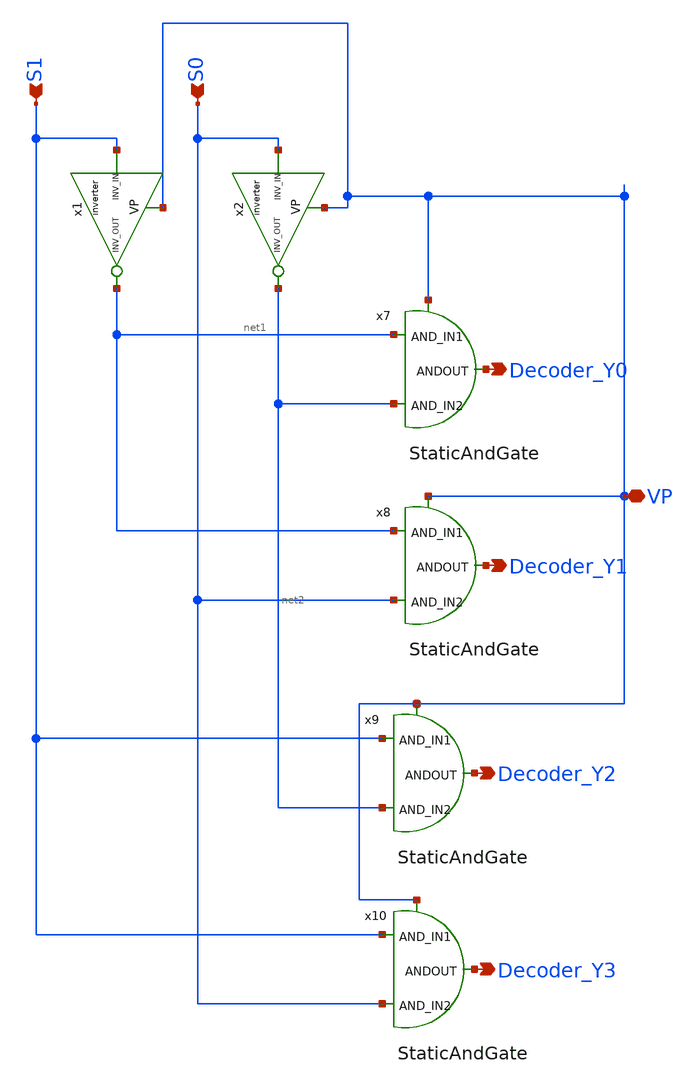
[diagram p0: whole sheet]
** sch_path: AllSymbols&Sch/Decoder/Decoder_2:4.sch
**.subckt Decoder_2:4 S0 Decoder_Y0 VP S1 Decoder_Y1 Decoder_Y2 Decoder_Y3
*.ipin S0
*.opin Decoder_Y0
*.iopin VP
*.ipin S1
*.opin Decoder_Y1
*.opin Decoder_Y2
*.opin Decoder_Y3
x7 Decoder_Y0 net1 net2 VP StaticAndGate
x8 Decoder_Y1 net1 S0 VP StaticAndGate
x9 Decoder_Y2 S1 net2 VP StaticAndGate
x10 Decoder_Y3 S1 S0 VP StaticAndGate
x1 VP net1 S1 inverter
x2 VP net2 S0 inverter
**.ends

* expanding   symbol:
*+  /home/safal/projects/GitHub_CMOS_4bit_ALU/AllSymbols&Sch/Gates/StaticAndGate.sym # of pins=4
** sym_path: AllSymbols&Sch/Gates/StaticAndGate.sym
** sch_path: AllSymbols&Sch/Gates/StaticAndGate.sch
.subckt StaticAndGate ANDOUT AND_IN1 AND_IN2 VP
*.ipin AND_IN1
*.opin ANDOUT
*.ipin AND_IN2
*.iopin VP
XM1 net2 AND_IN2 VP VP sky130_fd_pr__pfet_01v8 L=0.15 W=1 nf=1 ad='int((1 + 1)/2) * 1 / 1 * 0.29' as='int((1 + 2)/2) * 1 / 1 * 0.29'
+ pd='2*int((1 + 1)/2) * (1 / 1 + 0.29)' ps='2*int((1 + 2)/2) * (1 / 1 + 0.29)' nrd='0.29 / 1 ' nrs='0.29 / 1 '
+ sa=0 sb=0 sd=0 mult=1 m=1
XM2 net2 AND_IN1 net1 net1 sky130_fd_pr__nfet_01v8 L=0.15 W=2 nf=1 ad='int((1 + 1)/2) * 2 / 1 * 0.29'
+ as='int((1 + 2)/2) * 2 / 1 * 0.29' pd='2*int((1 + 1)/2) * (2 / 1 + 0.29)' ps='2*int((1 + 2)/2) * (2 / 1 + 0.29)'
+ nrd='0.29 / 2 ' nrs='0.29 / 2 ' sa=0 sb=0 sd=0 mult=1 m=1
XM3 net1 AND_IN2 GND GND sky130_fd_pr__nfet_01v8 L=0.15 W=2 nf=1 ad='int((1 + 1)/2) * 2 / 1 * 0.29' as='int((1 + 2)/2) * 2 / 1 * 0.29'
+ pd='2*int((1 + 1)/2) * (2 / 1 + 0.29)' ps='2*int((1 + 2)/2) * (2 / 1 + 0.29)' nrd='0.29 / 2 ' nrs='0.29 / 2 '
+ sa=0 sb=0 sd=0 mult=1 m=1
XM4 net2 AND_IN1 VP VP sky130_fd_pr__pfet_01v8 L=0.15 W=1 nf=1 ad='int((1 + 1)/2) * 1 / 1 * 0.29' as='int((1 + 2)/2) * 1 / 1 * 0.29'
+ pd='2*int((1 + 1)/2) * (1 / 1 + 0.29)' ps='2*int((1 + 2)/2) * (1 / 1 + 0.29)' nrd='0.29 / 1 ' nrs='0.29 / 1 '
+ sa=0 sb=0 sd=0 mult=1 m=1
x1 VP ANDOUT net2 inverter
.ends


* expanding   symbol:
*+  /home/safal/projects/GitHub_CMOS_4bit_ALU/AllSymbols&Sch/GenericSym/inverter.sym # of pins=3
** sym_path: AllSymbols&Sch/GenericSym/inverter.sym
** sch_path: AllSymbols&Sch/GenericSym/inverter.sch
.subckt inverter VP inv_out inv_in
*.ipin inv_in
*.opin inv_out
*.iopin VP
XM1 inv_out inv_in VP VP sky130_fd_pr__pfet_01v8 L=0.15 W=2 nf=1 ad='int((1 + 1)/2) * 2 / 1 * 0.29' as='int((1 + 2)/2) * 2 / 1 * 0.29'
+ pd='2*int((1 + 1)/2) * (2 / 1 + 0.29)' ps='2*int((1 + 2)/2) * (2 / 1 + 0.29)' nrd='0.29 / 2 ' nrs='0.29 / 2 '
+ sa=0 sb=0 sd=0 mult=1 m=1
XM2 inv_out inv_in GND GND sky130_fd_pr__nfet_01v8 L=0.15 W=1 nf=1 ad='int((1 + 1)/2) * 1 / 1 * 0.29'
+ as='int((1 + 2)/2) * 1 / 1 * 0.29' pd='2*int((1 + 1)/2) * (1 / 1 + 0.29)' ps='2*int((1 + 2)/2) * (1 / 1 + 0.29)'
+ nrd='0.29 / 1 ' nrs='0.29 / 1 ' sa=0 sb=0 sd=0 mult=1 m=1
.ends

.GLOBAL GND
.end
